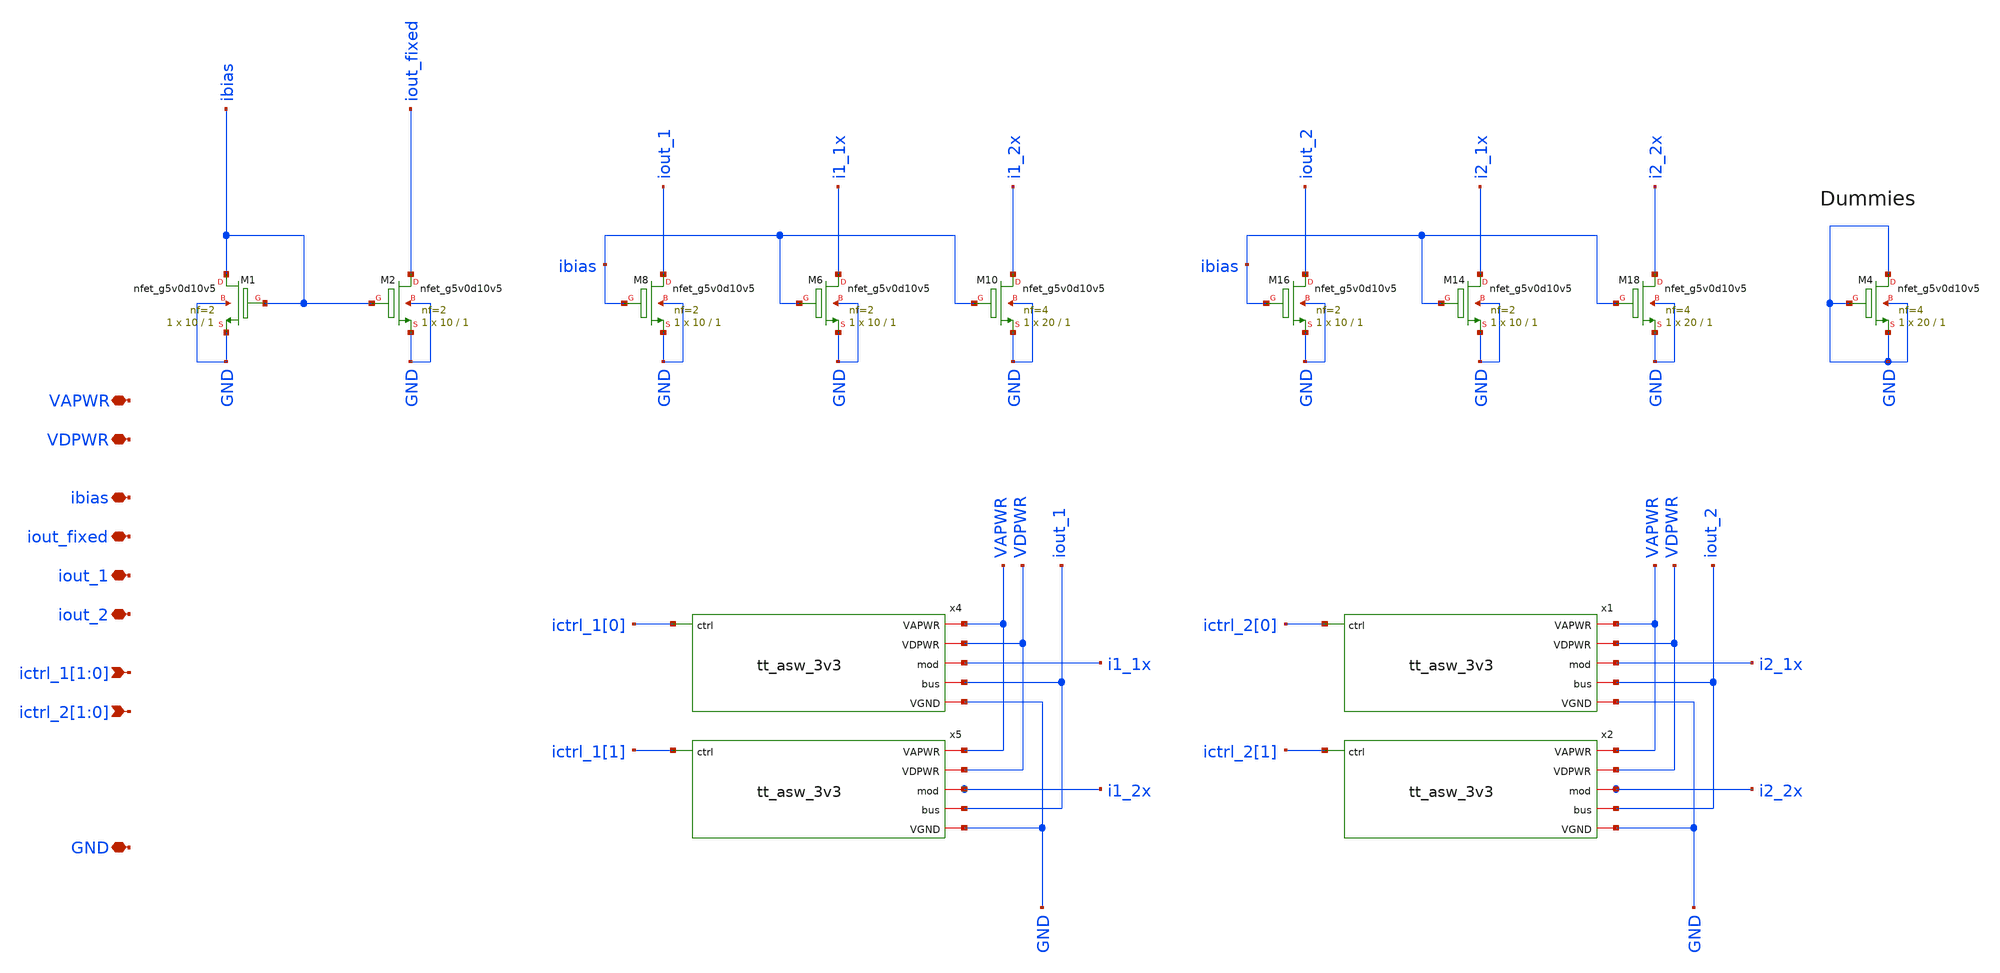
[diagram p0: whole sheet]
** sch_path: tt_um_mosbius/xschem/mirror_n.sch
**.subckt mirror_n ibias iout_fixed iout_1 ictrl_1[1],ictrl_1[0] ictrl_2[1],ictrl_2[0] iout_2 VAPWR
*+ VDPWR GND
*.iopin ibias
*.iopin iout_fixed
*.iopin iout_1
*.ipin ictrl_1[1],ictrl_1[0]
*.ipin ictrl_2[1],ictrl_2[0]
*.iopin iout_2
*.iopin VAPWR
*.iopin VDPWR
*.iopin GND
XM1 ibias ibias GND GND sky130_fd_pr__nfet_g5v0d10v5 L=1 W=10 nf=2 ad='int((nf+1)/2) * W/nf * 0.29' as='int((nf+2)/2) * W/nf * 0.29'
+ pd='2*int((nf+1)/2) * (W/nf + 0.29)' ps='2*int((nf+2)/2) * (W/nf + 0.29)' nrd='0.29 / W' nrs='0.29 / W'
+ sa=0 sb=0 sd=0 mult=1 m=1
XM2 iout_fixed ibias GND GND sky130_fd_pr__nfet_g5v0d10v5 L=1 W=10 nf=2 ad='int((nf+1)/2) * W/nf * 0.29'
+ as='int((nf+2)/2) * W/nf * 0.29' pd='2*int((nf+1)/2) * (W/nf + 0.29)' ps='2*int((nf+2)/2) * (W/nf + 0.29)'
+ nrd='0.29 / W' nrs='0.29 / W' sa=0 sb=0 sd=0 mult=1 m=1
XM6 i1_1x ibias GND GND sky130_fd_pr__nfet_g5v0d10v5 L=1 W=10 nf=2 ad='int((nf+1)/2) * W/nf * 0.29' as='int((nf+2)/2) * W/nf * 0.29'
+ pd='2*int((nf+1)/2) * (W/nf + 0.29)' ps='2*int((nf+2)/2) * (W/nf + 0.29)' nrd='0.29 / W' nrs='0.29 / W'
+ sa=0 sb=0 sd=0 mult=1 m=1
XM8 iout_1 ibias GND GND sky130_fd_pr__nfet_g5v0d10v5 L=1 W=10 nf=2 ad='int((nf+1)/2) * W/nf * 0.29'
+ as='int((nf+2)/2) * W/nf * 0.29' pd='2*int((nf+1)/2) * (W/nf + 0.29)' ps='2*int((nf+2)/2) * (W/nf + 0.29)'
+ nrd='0.29 / W' nrs='0.29 / W' sa=0 sb=0 sd=0 mult=1 m=1
XM10 i1_2x ibias GND GND sky130_fd_pr__nfet_g5v0d10v5 L=1 W=20 nf=4 ad='int((nf+1)/2) * W/nf * 0.29'
+ as='int((nf+2)/2) * W/nf * 0.29' pd='2*int((nf+1)/2) * (W/nf + 0.29)' ps='2*int((nf+2)/2) * (W/nf + 0.29)'
+ nrd='0.29 / W' nrs='0.29 / W' sa=0 sb=0 sd=0 mult=1 m=1
x4 GND VDPWR VAPWR ictrl_1[0] i1_1x iout_1 tt_asw_3v3
x5 GND VDPWR VAPWR ictrl_1[1] i1_2x iout_1 tt_asw_3v3
XM14 i2_1x ibias GND GND sky130_fd_pr__nfet_g5v0d10v5 L=1 W=10 nf=2 ad='int((nf+1)/2) * W/nf * 0.29'
+ as='int((nf+2)/2) * W/nf * 0.29' pd='2*int((nf+1)/2) * (W/nf + 0.29)' ps='2*int((nf+2)/2) * (W/nf + 0.29)'
+ nrd='0.29 / W' nrs='0.29 / W' sa=0 sb=0 sd=0 mult=1 m=1
XM16 iout_2 ibias GND GND sky130_fd_pr__nfet_g5v0d10v5 L=1 W=10 nf=2 ad='int((nf+1)/2) * W/nf * 0.29'
+ as='int((nf+2)/2) * W/nf * 0.29' pd='2*int((nf+1)/2) * (W/nf + 0.29)' ps='2*int((nf+2)/2) * (W/nf + 0.29)'
+ nrd='0.29 / W' nrs='0.29 / W' sa=0 sb=0 sd=0 mult=1 m=1
XM18 i2_2x ibias GND GND sky130_fd_pr__nfet_g5v0d10v5 L=1 W=20 nf=4 ad='int((nf+1)/2) * W/nf * 0.29'
+ as='int((nf+2)/2) * W/nf * 0.29' pd='2*int((nf+1)/2) * (W/nf + 0.29)' ps='2*int((nf+2)/2) * (W/nf + 0.29)'
+ nrd='0.29 / W' nrs='0.29 / W' sa=0 sb=0 sd=0 mult=1 m=1
x1 GND VDPWR VAPWR ictrl_2[0] i2_1x iout_2 tt_asw_3v3
x2 GND VDPWR VAPWR ictrl_2[1] i2_2x iout_2 tt_asw_3v3
XM4 GND GND GND GND sky130_fd_pr__nfet_g5v0d10v5 L=1 W=20 nf=4 ad='int((nf+1)/2) * W/nf * 0.29' as='int((nf+2)/2) * W/nf * 0.29'
+ pd='2*int((nf+1)/2) * (W/nf + 0.29)' ps='2*int((nf+2)/2) * (W/nf + 0.29)' nrd='0.29 / W' nrs='0.29 / W'
+ sa=0 sb=0 sd=0 mult=1 m=1
**.ends

* expanding   symbol:  tt_asw_3v3.sym # of pins=6
** sym_path: tt_asw_3v3.sym
** sch_path: tt_asw_3v3.sch
.subckt tt_asw_3v3 VGND VDPWR VAPWR ctrl mod bus
*.iopin mod
*.iopin bus
*.ipin ctrl
*.iopin VGND
*.iopin VDPWR
*.iopin VAPWR
XM1 tgon_n net2 VAPWR VAPWR sky130_fd_pr__pfet_g5v0d10v5 L=0.5 W=0.84 nf=1 ad='int((nf+1)/2) * W/nf * 0.29'
+ as='int((nf+2)/2) * W/nf * 0.29' pd='2*int((nf+1)/2) * (W/nf + 0.29)' ps='2*int((nf+2)/2) * (W/nf + 0.29)'
+ nrd='0.29 / W' nrs='0.29 / W' sa=0 sb=0 sd=0 mult=1 m=1
XM2 tgon_n net2 VGND VGND sky130_fd_pr__nfet_g5v0d10v5 L=0.5 W=0.42 nf=1 ad='int((nf+1)/2) * W/nf * 0.29'
+ as='int((nf+2)/2) * W/nf * 0.29' pd='2*int((nf+1)/2) * (W/nf + 0.29)' ps='2*int((nf+2)/2) * (W/nf + 0.29)'
+ nrd='0.29 / W' nrs='0.29 / W' sa=0 sb=0 sd=0 mult=1 m=1
XM3 tgon net1 VAPWR VAPWR sky130_fd_pr__pfet_g5v0d10v5 L=0.5 W=0.84 nf=1 ad='int((nf+1)/2) * W/nf * 0.29'
+ as='int((nf+2)/2) * W/nf * 0.29' pd='2*int((nf+1)/2) * (W/nf + 0.29)' ps='2*int((nf+2)/2) * (W/nf + 0.29)'
+ nrd='0.29 / W' nrs='0.29 / W' sa=0 sb=0 sd=0 mult=1 m=1
XM4 tgon net1 VGND VGND sky130_fd_pr__nfet_g5v0d10v5 L=0.5 W=0.42 nf=1 ad='int((nf+1)/2) * W/nf * 0.29'
+ as='int((nf+2)/2) * W/nf * 0.29' pd='2*int((nf+1)/2) * (W/nf + 0.29)' ps='2*int((nf+2)/2) * (W/nf + 0.29)'
+ nrd='0.29 / W' nrs='0.29 / W' sa=0 sb=0 sd=0 mult=1 m=1
XM5 bus tgon_n mod VAPWR sky130_fd_pr__pfet_g5v0d10v5 L=0.5 W=180 nf=18 ad='int((nf+1)/2) * W/nf * 0.29'
+ as='int((nf+2)/2) * W/nf * 0.29' pd='2*int((nf+1)/2) * (W/nf + 0.29)' ps='2*int((nf+2)/2) * (W/nf + 0.29)'
+ nrd='0.29 / W' nrs='0.29 / W' sa=0 sb=0 sd=0 mult=1 m=1
XM6 bus tgon mod VGND sky130_fd_pr__nfet_g5v0d10v5 L=0.5 W=60 nf=12 ad='int((nf+1)/2) * W/nf * 0.29'
+ as='int((nf+2)/2) * W/nf * 0.29' pd='2*int((nf+1)/2) * (W/nf + 0.29)' ps='2*int((nf+2)/2) * (W/nf + 0.29)'
+ nrd='0.29 / W' nrs='0.29 / W' sa=0 sb=0 sd=0 mult=1 m=1
XM7 ctrl_n ctrl VGND VGND sky130_fd_pr__nfet_01v8 L=0.15 W=0.42 nf=1 ad='int((nf+1)/2) * W/nf * 0.29'
+ as='int((nf+2)/2) * W/nf * 0.29' pd='2*int((nf+1)/2) * (W/nf + 0.29)' ps='2*int((nf+2)/2) * (W/nf + 0.29)'
+ nrd='0.29 / W' nrs='0.29 / W' sa=0 sb=0 sd=0 mult=1 m=1
XM8 ctrl_n ctrl VDPWR VDPWR sky130_fd_pr__pfet_01v8_hvt L=0.15 W=1 nf=1 ad='int((nf+1)/2) * W/nf * 0.29'
+ as='int((nf+2)/2) * W/nf * 0.29' pd='2*int((nf+1)/2) * (W/nf + 0.29)' ps='2*int((nf+2)/2) * (W/nf + 0.29)'
+ nrd='0.29 / W' nrs='0.29 / W' sa=0 sb=0 sd=0 mult=1 m=1
XM9 net1 ctrl VGND VGND sky130_fd_pr__nfet_g5v0d10v5 L=0.5 W=0.42 nf=1 ad='int((nf+1)/2) * W/nf * 0.29'
+ as='int((nf+2)/2) * W/nf * 0.29' pd='2*int((nf+1)/2) * (W/nf + 0.29)' ps='2*int((nf+2)/2) * (W/nf + 0.29)'
+ nrd='0.29 / W' nrs='0.29 / W' sa=0 sb=0 sd=0 mult=1 m=1
XM10 net2 ctrl_n VGND VGND sky130_fd_pr__nfet_g5v0d10v5 L=0.5 W=0.42 nf=1 ad='int((nf+1)/2) * W/nf * 0.29'
+ as='int((nf+2)/2) * W/nf * 0.29' pd='2*int((nf+1)/2) * (W/nf + 0.29)' ps='2*int((nf+2)/2) * (W/nf + 0.29)'
+ nrd='0.29 / W' nrs='0.29 / W' sa=0 sb=0 sd=0 mult=1 m=1
XM11 net1 net2 net3 VAPWR sky130_fd_pr__pfet_g5v0d10v5 L=0.5 W=0.42 nf=1 ad='int((nf+1)/2) * W/nf * 0.29'
+ as='int((nf+2)/2) * W/nf * 0.29' pd='2*int((nf+1)/2) * (W/nf + 0.29)' ps='2*int((nf+2)/2) * (W/nf + 0.29)'
+ nrd='0.29 / W' nrs='0.29 / W' sa=0 sb=0 sd=0 mult=1 m=1
XM12 net2 net1 net4 VAPWR sky130_fd_pr__pfet_g5v0d10v5 L=0.5 W=0.42 nf=1 ad='int((nf+1)/2) * W/nf * 0.29'
+ as='int((nf+2)/2) * W/nf * 0.29' pd='2*int((nf+1)/2) * (W/nf + 0.29)' ps='2*int((nf+2)/2) * (W/nf + 0.29)'
+ nrd='0.29 / W' nrs='0.29 / W' sa=0 sb=0 sd=0 mult=1 m=1
XM13 net3 net1 VAPWR VAPWR sky130_fd_pr__pfet_g5v0d10v5 L=0.5 W=0.42 nf=1 ad='int((nf+1)/2) * W/nf * 0.29'
+ as='int((nf+2)/2) * W/nf * 0.29' pd='2*int((nf+1)/2) * (W/nf + 0.29)' ps='2*int((nf+2)/2) * (W/nf + 0.29)'
+ nrd='0.29 / W' nrs='0.29 / W' sa=0 sb=0 sd=0 mult=1 m=1
XM14 net4 net2 VAPWR VAPWR sky130_fd_pr__pfet_g5v0d10v5 L=0.5 W=0.42 nf=1 ad='int((nf+1)/2) * W/nf * 0.29'
+ as='int((nf+2)/2) * W/nf * 0.29' pd='2*int((nf+1)/2) * (W/nf + 0.29)' ps='2*int((nf+2)/2) * (W/nf + 0.29)'
+ nrd='0.29 / W' nrs='0.29 / W' sa=0 sb=0 sd=0 mult=1 m=1
.ends

.end
